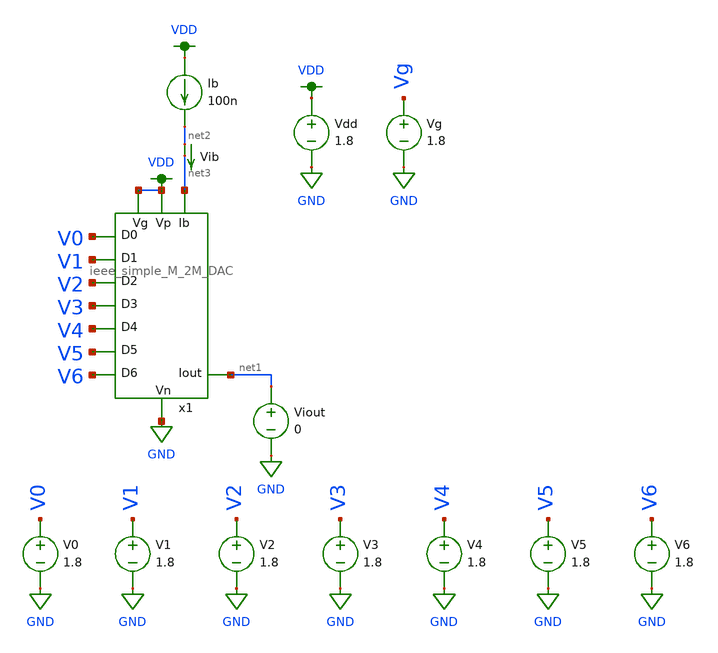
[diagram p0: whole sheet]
** sch_path: schematics/ieee_DAC_mc_simulation.sch
**.subckt ieee_DAC_mc_simulation
Ib VDD net2 100n
Vdd VDD GND 1.8
V1 V1 GND 1.8
V2 V2 GND 1.8
V3 V3 GND 1.8
V4 V4 GND 1.8
V5 V5 GND 1.8
V6 V6 GND 1.8
V0 V0 GND 1.8
Vg Vg GND 1.8
Viout net1 GND 0
x1 VDD net1 GND V1 V0 V2 V3 V4 V5 V6 VDD net3 ieee_simple_M_2M_DAC
Vib net2 net3 0
.save i(vib)
**** begin user architecture code

.option wnflag=1
.param MC_SWITCH=1.0
.lib ~/skywater/skywater-pdk/libraries/sky130_fd_pr_ngspice/latest/models/sky130.lib.spice tt



.control
set wr_vecnames
set wr_singlescale

let mc_runs = 10
let run = 1
dowhile run <= mc_runs

  let code = 0
  while code < 128
    if floor(code / 1) eq 0
      let b0 = 0
    else
      let b0 = (floor(code / 1) % 2) * 1.8
    end
    if floor(code / 2) eq 0
      let b1 = 0
    else
      let b1 = (floor(code / 2) % 2) * 1.8
    end
    if floor(code / 4) eq 0
      let b2 = 0
    else
      let b2 = (floor(code / 4) % 2) * 1.8
    end
    if floor(code / 8) eq 0
      let b3 = 0
    else
      let b3 = (floor(code / 8) % 2) * 1.8
    end
    if floor(code / 16) eq 0
      let b4 = 0
    else
      let b4 = (floor(code / 16) % 2) * 1.8
    end
    if floor(code / 32) eq 0
      let b5 = 0
    else
      let b5 = (floor(code / 32) % 2) * 1.8
    end
    if floor(code / 64) eq 0
      let b6 = 0
    else
      let b6 = (floor(code / 64) % 2) * 1.8
    end

    alter V0 $&b0
    alter V1 $&b1
    alter V2 $&b2
    alter V3 $&b3
    alter V4 $&b4
    alter V5 $&b5
    alter V6 $&b6
    save all
    op

    wrdata ~/dev/git/7-bit-D-A-converter-MP4-MADVLSI/schematics/simulations/ieee_DAC/simulation_results/ieee_DAC_{$&run}.txt
+ V0 V1 V2 V3 V4 V5 V6 i(Vib) i(Viout)
    if code eq 0
      set appendwrite
      set wr_vecnames = FALSE
    end
    reset
    let code = code + 1
  end

  set appendwrite = FALSE
  set wr_vecnames
  let run = run + 1
end
quit
.endc

**** end user architecture code
**.ends
.GLOBAL VDD
.GLOBAL GND
.end
